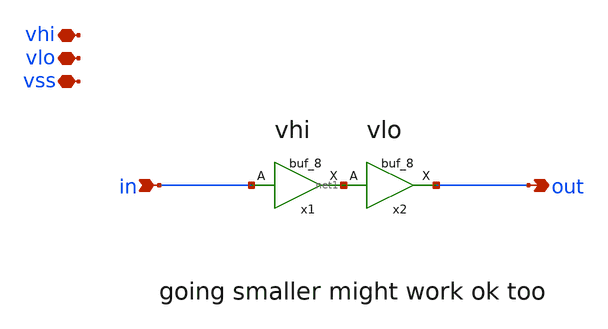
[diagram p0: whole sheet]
** sch_path: xschem/level_shifter/level_down_shifter.sch
**.subckt level_down_shifter in vss vhi out vlo
*.ipin in
*.iopin vss
*.iopin vhi
*.opin out
*.iopin vlo
x1 in vss vss vhi vhi net1 sky130_fd_sc_hd__buf_8
x2 net1 vss vss vlo vlo out sky130_fd_sc_hd__buf_8
**.ends
.end
